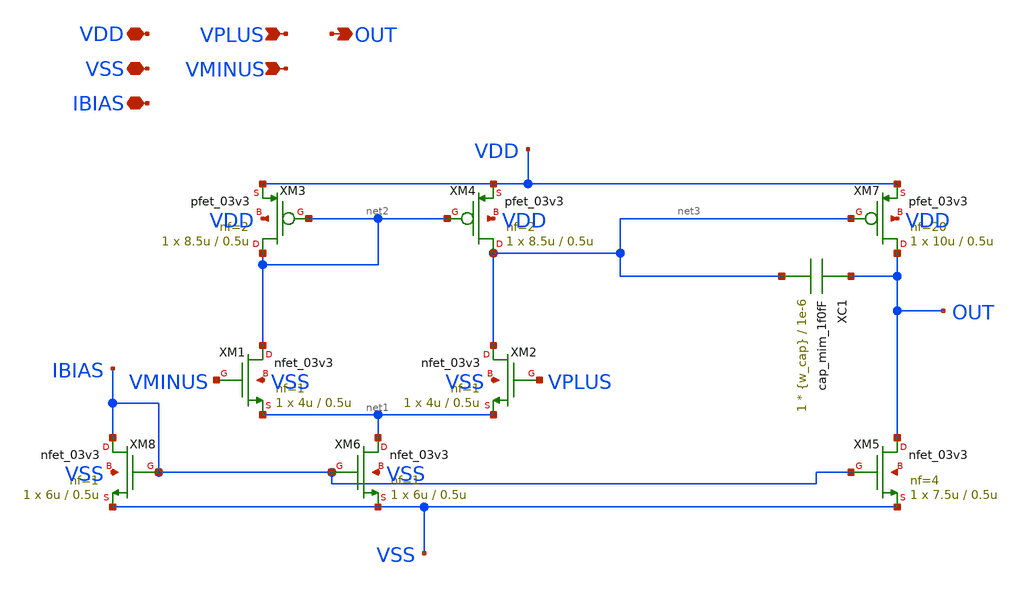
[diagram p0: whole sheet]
** sch_path: xschem/op_amp.sch
**.subckt op_amp VDD VSS VPLUS VMINUS OUT IBIAS
*.iopin VDD
*.iopin VSS
*.ipin VPLUS
*.ipin VMINUS
*.opin OUT
*.iopin IBIAS
XM1 net2 VMINUS net1 VSS nfet_03v3 L=0.5u W=4u nf=1 ad='int((nf+1)/2) * W/nf * 0.18u' as='int((nf+2)/2) * W/nf * 0.18u'
+ pd='2*int((nf+1)/2) * (W/nf + 0.18u)' ps='2*int((nf+2)/2) * (W/nf + 0.18u)' nrd='0.18u / W' nrs='0.18u / W'
+ sa=0 sb=0 sd=0 m=1
XM2 net3 VPLUS net1 VSS nfet_03v3 L=0.5u W=4u nf=1 ad='int((nf+1)/2) * W/nf * 0.18u' as='int((nf+2)/2) * W/nf * 0.18u'
+ pd='2*int((nf+1)/2) * (W/nf + 0.18u)' ps='2*int((nf+2)/2) * (W/nf + 0.18u)' nrd='0.18u / W' nrs='0.18u / W'
+ sa=0 sb=0 sd=0 m=1
XM3 net2 net2 VDD VDD pfet_03v3 L=0.5u W=8.5u nf=2 ad='int((nf+1)/2) * W/nf * 0.18u' as='int((nf+2)/2) * W/nf * 0.18u'
+ pd='2*int((nf+1)/2) * (W/nf + 0.18u)' ps='2*int((nf+2)/2) * (W/nf + 0.18u)' nrd='0.18u / W' nrs='0.18u / W'
+ sa=0 sb=0 sd=0 m=1
XM4 net3 net2 VDD VDD pfet_03v3 L=0.5u W=8.5u nf=2 ad='int((nf+1)/2) * W/nf * 0.18u' as='int((nf+2)/2) * W/nf * 0.18u'
+ pd='2*int((nf+1)/2) * (W/nf + 0.18u)' ps='2*int((nf+2)/2) * (W/nf + 0.18u)' nrd='0.18u / W' nrs='0.18u / W'
+ sa=0 sb=0 sd=0 m=1
XM6 net1 IBIAS VSS VSS nfet_03v3 L=0.5u W=6u nf=1 ad='int((nf+1)/2) * W/nf * 0.18u' as='int((nf+2)/2) * W/nf * 0.18u'
+ pd='2*int((nf+1)/2) * (W/nf + 0.18u)' ps='2*int((nf+2)/2) * (W/nf + 0.18u)' nrd='0.18u / W' nrs='0.18u / W'
+ sa=0 sb=0 sd=0 m=1
XM7 OUT net3 VDD VDD pfet_03v3 L=0.5u W=10u nf=20 ad='int((nf+1)/2) * W/nf * 0.18u' as='int((nf+2)/2) * W/nf * 0.18u'
+ pd='2*int((nf+1)/2) * (W/nf + 0.18u)' ps='2*int((nf+2)/2) * (W/nf + 0.18u)' nrd='0.18u / W' nrs='0.18u / W'
+ sa=0 sb=0 sd=0 m=1
XM8 IBIAS IBIAS VSS VSS nfet_03v3 L=0.5u W=6u nf=1 ad='int((nf+1)/2) * W/nf * 0.18u' as='int((nf+2)/2) * W/nf * 0.18u'
+ pd='2*int((nf+1)/2) * (W/nf + 0.18u)' ps='2*int((nf+2)/2) * (W/nf + 0.18u)' nrd='0.18u / W' nrs='0.18u / W'
+ sa=0 sb=0 sd=0 m=1
XM5 OUT IBIAS VSS net4 nfet_03v3 L=0.5u W=7.5u nf=4 ad='int((nf+1)/2) * W/nf * 0.18u' as='int((nf+2)/2) * W/nf * 0.18u'
+ pd='2*int((nf+1)/2) * (W/nf + 0.18u)' ps='2*int((nf+2)/2) * (W/nf + 0.18u)' nrd='0.18u / W' nrs='0.18u / W'
+ sa=0 sb=0 sd=0 m=1
XC1 OUT net3 cap_mim_1f0fF c_width={w_cap} c_length=1e-6 m=1
**.ends
.end
